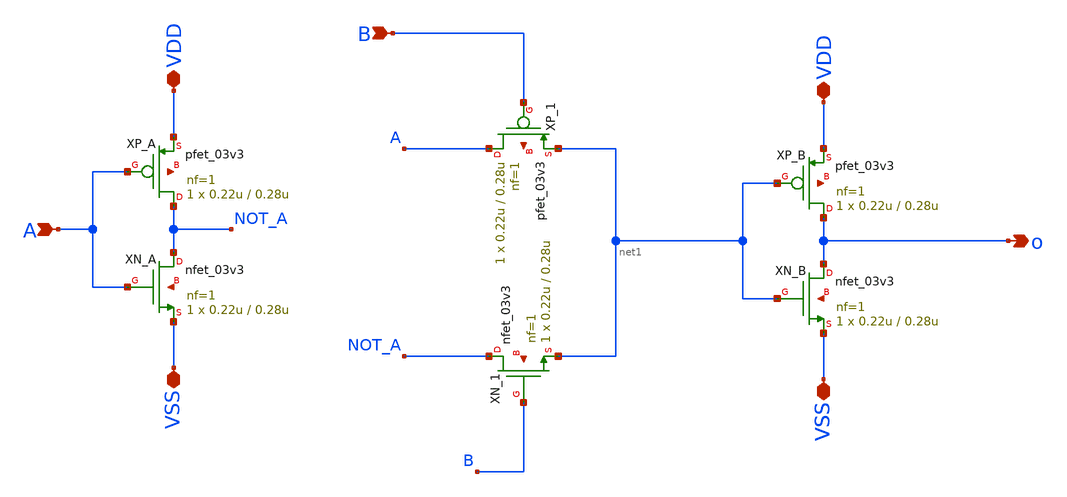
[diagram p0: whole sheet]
** sch_path: schematics/pass6_xor.sch
**.subckt pass6_xor VDD VSS A VDD VSS VSS o B
*.iopin VDD
*.iopin VSS
*.ipin A
*.iopin VDD
*.iopin VSS
*.iopin VSS
*.opin o
*.ipin B
XP_A NOT_A A VDD net2 pfet_03v3 L=0.28u W=0.22u nf=1 ad='int((nf+1)/2) * W/nf * 0.18u' as='int((nf+2)/2) * W/nf * 0.18u'
+ pd='2*int((nf+1)/2) * (W/nf + 0.18u)' ps='2*int((nf+2)/2) * (W/nf + 0.18u)' nrd='0.18u / W' nrs='0.18u / W'
+ sa=0 sb=0 sd=0 m=1
XN_A NOT_A A VSS net3 nfet_03v3 L=0.28u W=0.22u nf=1 ad='int((nf+1)/2) * W/nf * 0.18u' as='int((nf+2)/2) * W/nf * 0.18u'
+ pd='2*int((nf+1)/2) * (W/nf + 0.18u)' ps='2*int((nf+2)/2) * (W/nf + 0.18u)' nrd='0.18u / W' nrs='0.18u / W'
+ sa=0 sb=0 sd=0 m=1
XP_B o net1 VDD net4 pfet_03v3 L=0.28u W=0.22u nf=1 ad='int((nf+1)/2) * W/nf * 0.18u' as='int((nf+2)/2) * W/nf * 0.18u'
+ pd='2*int((nf+1)/2) * (W/nf + 0.18u)' ps='2*int((nf+2)/2) * (W/nf + 0.18u)' nrd='0.18u / W' nrs='0.18u / W'
+ sa=0 sb=0 sd=0 m=1
XN_B o net1 VSS net5 nfet_03v3 L=0.28u W=0.22u nf=1 ad='int((nf+1)/2) * W/nf * 0.18u' as='int((nf+2)/2) * W/nf * 0.18u'
+ pd='2*int((nf+1)/2) * (W/nf + 0.18u)' ps='2*int((nf+2)/2) * (W/nf + 0.18u)' nrd='0.18u / W' nrs='0.18u / W'
+ sa=0 sb=0 sd=0 m=1
XP_1 A B net1 net6 pfet_03v3 L=0.28u W=0.22u nf=1 ad='int((nf+1)/2) * W/nf * 0.18u' as='int((nf+2)/2) * W/nf * 0.18u'
+ pd='2*int((nf+1)/2) * (W/nf + 0.18u)' ps='2*int((nf+2)/2) * (W/nf + 0.18u)' nrd='0.18u / W' nrs='0.18u / W'
+ sa=0 sb=0 sd=0 m=1
XN_1 NOT_A B net1 net7 nfet_03v3 L=0.28u W=0.22u nf=1 ad='int((nf+1)/2) * W/nf * 0.18u' as='int((nf+2)/2) * W/nf * 0.18u'
+ pd='2*int((nf+1)/2) * (W/nf + 0.18u)' ps='2*int((nf+2)/2) * (W/nf + 0.18u)' nrd='0.18u / W' nrs='0.18u / W'
+ sa=0 sb=0 sd=0 m=1
**.ends
.end
